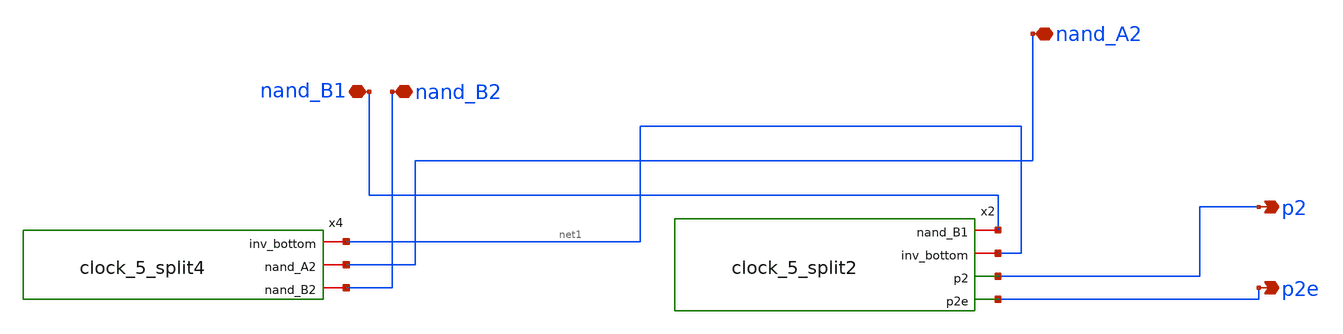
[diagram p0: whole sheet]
** sch_path: 5_Design/4_Layout/Team 5/splitUpSimulationsAndSchematics/clock_5_splitTop2.sch
* IHP-GmbH/IHP-Open-PDK/ihp-sg13g2/libs.tech/xschem/sg13g2_stdcells/sg13g2_inv_4.sch:
* Copyright 2023 IHP PDK Authors
* Licensed under the Apache License, Version 2.0 (the "License");
**.subckt clock_5_splitTop2 p2 p2e nand_B2 nand_B1 nand_A2
*.opin p2
*.opin p2e
*.iopin nand_B2
*.iopin nand_B1
*.iopin nand_A2
x2 nand_B1 net1 p2 p2e clock_5_split2
x4 net1 nand_A2 nand_B2 clock_5_split4
**.ends

* expanding   symbol:  /foss/designs/clock_5_split2.sym # of pins=4
** sym_path: 5_Design/4_Layout/Team 5/splitUpSimulationsAndSchematics/clock_5_split2.sym
** sch_path: 5_Design/4_Layout/Team 5/splitUpSimulationsAndSchematics/clock_5_split2.sch
.subckt clock_5_split2 nand_B1 inv_bottom p2 p2e
*.opin p2
*.opin p2e
*.iopin inv_bottom
*.iopin nand_B1
x19 a2 inv_bottom VDD VSS sg13g2_inv_4
x20 p2e a2 VDD VSS sg13g2_inv_4
x21 nand_B1 p2e VDD VSS sg13g2_inv_4
x23 net2 net1 VDD VSS sg13g2_inv_4
x12 p2 net2 VDD VSS sg13g2_inv_8
x15 net1 a2 nand_B1 VDD VSS sg13g2_nand2_2
.ends


* expanding   symbol:  /foss/designs/clock_5_split4.sym # of pins=3
** sym_path: 5_Design/4_Layout/Team 5/xschem/clock_5_split4.sym
** sch_path: 5_Design/4_Layout/Team 5/xschem/clock_5_split4.sch
.subckt clock_5_split4 inv_bottom nand_A2 nand_B2
*.iopin inv_bottom
*.iopin nand_A2
*.iopin nand_B2
x16 net2 net1 VDD VSS sg13g2_inv_4
x17 net3 net2 VDD VSS sg13g2_inv_4
x18 inv_bottom net3 VDD VSS sg13g2_inv_4
x10 net1 nand_A2 nand_B2 VDD VSS sg13g2_nand2_2
.ends


* expanding   symbol:  sg13g2_stdcells/sg13g2_inv_4.sym # of pins=2
** sym_path: sg13g2_stdcells/sg13g2_inv_4.sym
** sch_path: sg13g2_stdcells/sg13g2_inv_4.sch
.subckt sg13g2_inv_4 Y A VDD VSS
*.ipin A
*.opin Y
*.iopin VDD
*.iopin VSS
XM1 Y A VSS VSS sg13_lv_nmos w=2.96u l=130.00n ng=4 m=1 mm_ok=1
XM2 Y A VDD VDD sg13_lv_pmos w=4.48u l=130.00n ng=4 m=1 mm_ok=1
.ends


* expanding   symbol:  sg13g2_stdcells/sg13g2_inv_8.sym # of pins=2
** sym_path: sg13g2_stdcells/sg13g2_inv_8.sym
** sch_path: sg13g2_stdcells/sg13g2_inv_8.sch
.subckt sg13g2_inv_8 Y A VDD VSS
*.opin Y
*.ipin A
*.iopin VDD
*.iopin VSS
XM1 Y A VSS VSS sg13_lv_nmos w=5.92u l=130.00n ng=8 m=1 mm_ok=1
XM2 Y A VDD VDD sg13_lv_pmos w=8.96u l=130.00n ng=8 m=1 mm_ok=1
.ends


* expanding   symbol:  sg13g2_stdcells/sg13g2_nand2_2.sym # of pins=3
** sym_path: sg13g2_stdcells/sg13g2_nand2_2.sym
** sch_path: sg13g2_stdcells/sg13g2_nand2_2.sch
.subckt sg13g2_nand2_2 Y A B VDD VSS
*.iopin VDD
*.iopin VSS
*.opin Y
*.ipin B
*.ipin A
XM1 Y A net1 VSS sg13_lv_nmos w=1.44u l=130.00n ng=2 m=1 mm_ok=1
XM2 net1 B VSS VSS sg13_lv_nmos w=1.44u l=130.00n ng=2 m=1 mm_ok=1
XM3 Y A VDD VDD sg13_lv_pmos w=2.24u l=130.00n ng=2 m=1 mm_ok=1
XM4 Y B VDD VDD sg13_lv_pmos w=2.24u l=130.00n ng=2 m=1 mm_ok=1
.ends

.end
